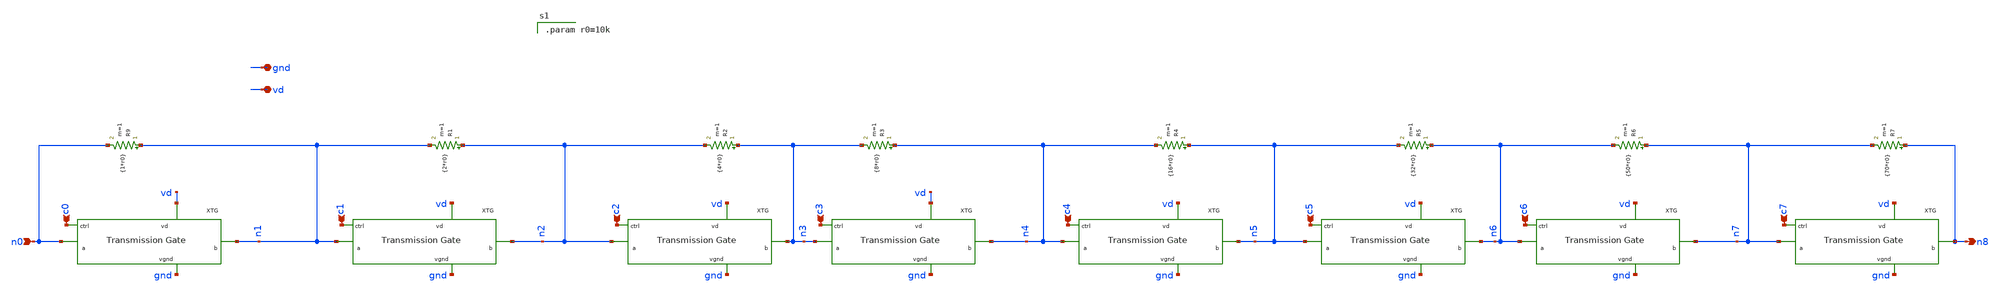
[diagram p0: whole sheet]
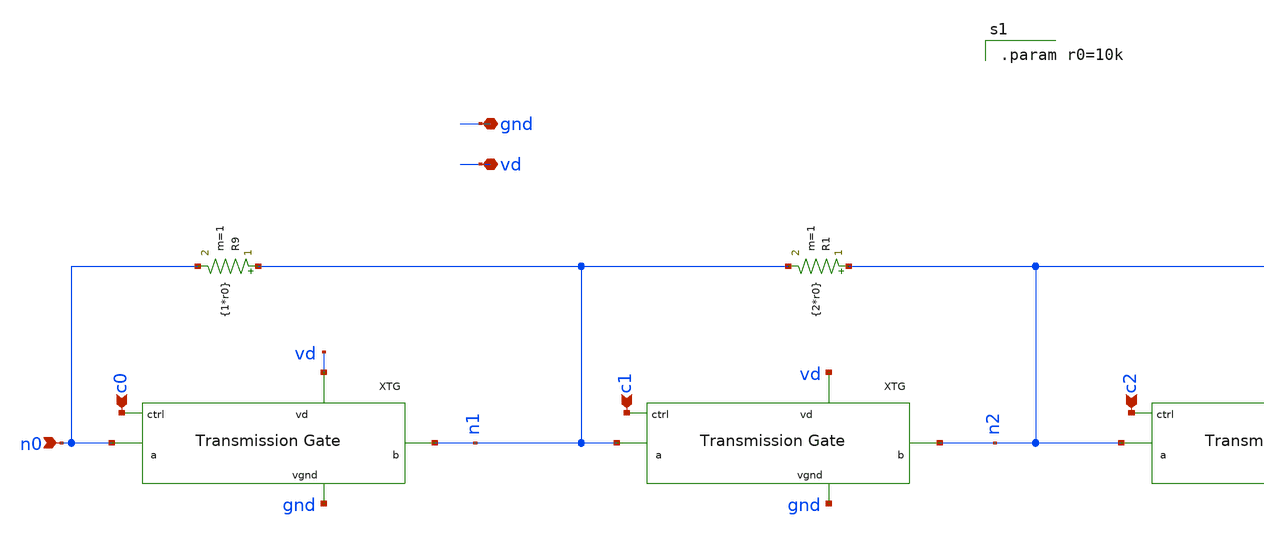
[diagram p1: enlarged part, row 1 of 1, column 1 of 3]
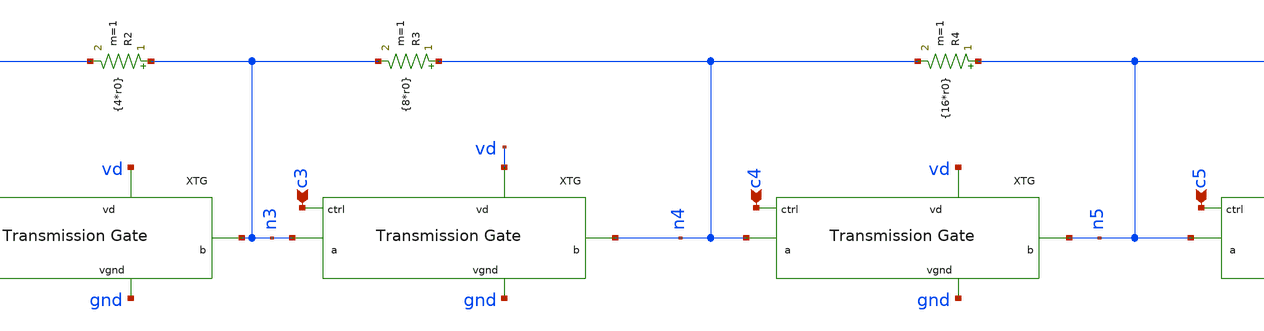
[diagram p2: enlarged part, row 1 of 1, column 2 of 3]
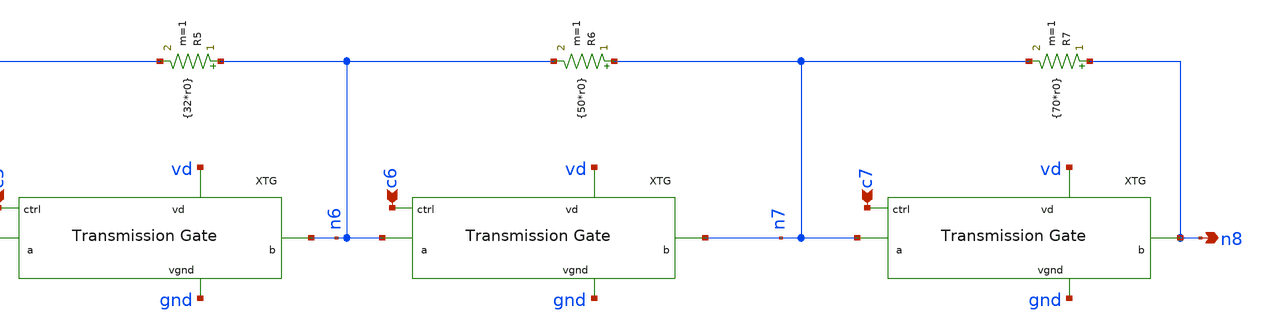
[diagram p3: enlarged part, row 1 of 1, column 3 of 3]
** sch_path: xschem/digpot.sch
**.subckt digpot gnd vd c0 c1 n0 c2 c3 c4 c5 c6 c7 n8
*.iopin gnd
*.iopin vd
*.ipin c0
*.ipin c1
*.ipin n0
*.ipin c2
*.ipin c3
*.ipin c4
*.ipin c5
*.ipin c6
*.ipin c7
*.opin n8
R9 n1 n0 {1*r0} m=1
x9 c0 vd n1 gnd n0 tg
x10 c1 vd n2 gnd n1 tg
x1 c2 vd n3 gnd n2 tg
x2 c3 vd n4 gnd n3 tg
x3 c4 vd n5 gnd n4 tg
x4 c5 vd n6 gnd n5 tg
x5 c6 vd n7 gnd n6 tg
x6 c7 vd n8 gnd n7 tg
R1 n2 n1 {2*r0} m=1
R2 n3 n2 {4*r0} m=1
R3 n4 n3 {8*r0} m=1
R4 n5 n4 {16*r0} m=1
R5 n6 n5 {32*r0} m=1
R6 n7 n6 {50*r0} m=1
R7 n8 n7 {70*r0} m=1
**** begin user architecture code

.param r0=10k

**** end user architecture code
**.ends

* expanding   symbol:  projects/dpga-ieee-sscs-contest/xschem/tg.sym # of pins=5
** sym_path: projects/dpga-ieee-sscs-contest/xschem/tg.sym
** sch_path: projects/dpga-ieee-sscs-contest/xschem/tg.sch
.subckt tg ctrl vd b vgnd a
*.iopin vd
*.iopin vgnd
*.iopin b
*.iopin a
*.ipin ctrl
XM2 b nctrl a vd sky130_fd_pr__pfet_01v8 L=0.15 W=60 nf=12 ad='int((nf+1)/2) * W/nf * 0.29' as='int((nf+2)/2) * W/nf * 0.29'
+ pd='2*int((nf+1)/2) * (W/nf + 0.29)' ps='2*int((nf+2)/2) * (W/nf + 0.29)' nrd='0.29 / W' nrs='0.29 / W'
+ sa=0 sb=0 sd=0 mult=1 m=1
XM1 a ctrl b vgnd sky130_fd_pr__nfet_01v8 L=0.15 W=60 nf=12 ad='int((nf+1)/2) * W/nf * 0.29' as='int((nf+2)/2) * W/nf * 0.29'
+ pd='2*int((nf+1)/2) * (W/nf + 0.29)' ps='2*int((nf+2)/2) * (W/nf + 0.29)' nrd='0.29 / W' nrs='0.29 / W'
+ sa=0 sb=0 sd=0 mult=1 m=1
XM3 nctrl ctrl vgnd vgnd sky130_fd_pr__nfet_01v8 L=0.15 W=1 nf=1 ad='int((nf+1)/2) * W/nf * 0.29' as='int((nf+2)/2) * W/nf * 0.29'
+ pd='2*int((nf+1)/2) * (W/nf + 0.29)' ps='2*int((nf+2)/2) * (W/nf + 0.29)' nrd='0.29 / W' nrs='0.29 / W'
+ sa=0 sb=0 sd=0 mult=1 m=1
XM4 nctrl ctrl vd vd sky130_fd_pr__pfet_01v8 L=0.15 W=3 nf=1 ad='int((nf+1)/2) * W/nf * 0.29' as='int((nf+2)/2) * W/nf * 0.29'
+ pd='2*int((nf+1)/2) * (W/nf + 0.29)' ps='2*int((nf+2)/2) * (W/nf + 0.29)' nrd='0.29 / W' nrs='0.29 / W'
+ sa=0 sb=0 sd=0 mult=1 m=1
.ends

.end
